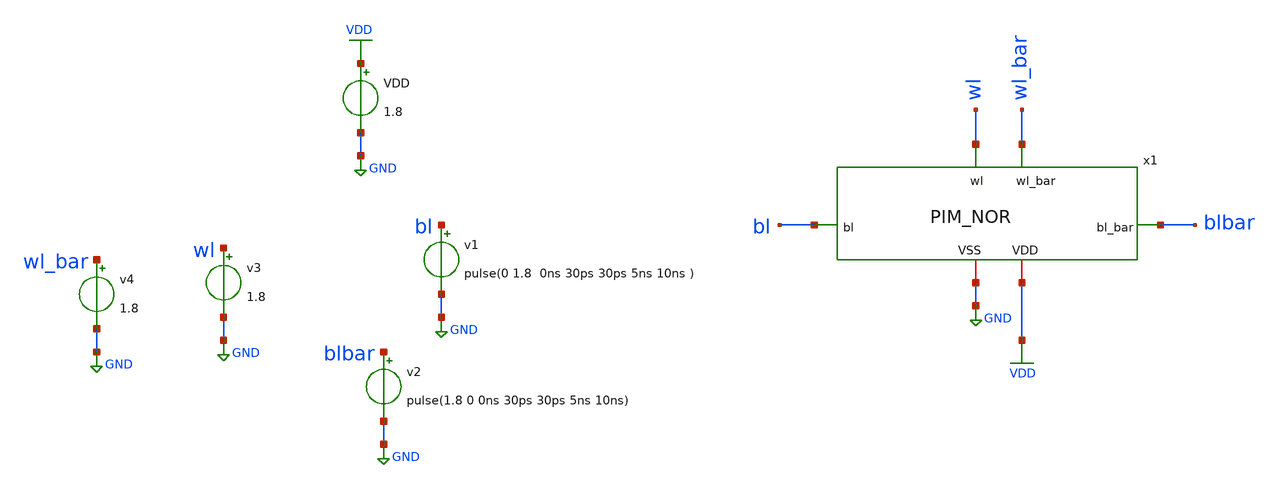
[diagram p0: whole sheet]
** sch_path: nikhil/SRAM/6T_PIM_TEST_SYMBOL.sch
**.subckt 6T_PIM_TEST_SYMBOL
x1 wl wl_bar VDD bl blbar GND PIM_NOR
VDD VDD GND 1.8
v1 bl GND pulse(0 1.8 0ns 30ps 30ps 5ns 10ns )
v3 wl GND 1.8
v2 blbar GND pulse(1.8 0 0ns 30ps 30ps 5ns 10ns)
v4 wl_bar GND 1.8
**** begin user architecture code

.tran


.options wnflag=1
.include /pdk/open_pdks/sources/sky130-pdk/libraries/sky130_fd_pr/latest/cells/nfet_01v8/sky130_fd_pr__nfet_01v8__tt.corner.spice
.include /pdk/open_pdks/sources/sky130-pdk/libraries/sky130_fd_pr/latest/cells/nfet_01v8_lvt/sky130_fd_pr__nfet_01v8_lvt__tt.corner.spice
.include /pdk/open_pdks/sources/sky130-pdk/libraries/sky130_fd_pr/latest/cells/pfet_01v8/sky130_fd_pr__pfet_01v8__tt.corner.spice
.include /pdk/open_pdks/sources/sky130-pdk/libraries/sky130_fd_pr/latest/cells/nfet_03v3_nvt/sky130_fd_pr__nfet_03v3_nvt__tt.corner.spice
.include /pdk/open_pdks/sources/sky130-pdk/libraries/sky130_fd_pr/latest/cells/nfet_05v0_nvt/sky130_fd_pr__nfet_05v0_nvt__tt.corner.spice
.include /pdk/open_pdks/sources/sky130-pdk/libraries/sky130_fd_pr/latest/cells/esd_nfet_01v8/sky130_fd_pr__esd_nfet_01v8__tt.corner.spice
.include /pdk/open_pdks/sources/sky130-pdk/libraries/sky130_fd_pr/latest/cells/pfet_01v8_lvt/sky130_fd_pr__pfet_01v8_lvt__tt.corner.spice
.include /pdk/open_pdks/sources/sky130-pdk/libraries/sky130_fd_pr/latest/cells/pfet_01v8_hvt/sky130_fd_pr__pfet_01v8_hvt__tt.corner.spice
.include /pdk/open_pdks/sources/sky130-pdk/libraries/sky130_fd_pr/latest/cells/esd_pfet_g5v0d10v5/sky130_fd_pr__esd_pfet_g5v0d10v5__tt.corner.spice
.include /pdk/open_pdks/sources/sky130-pdk/libraries/sky130_fd_pr/latest/cells/pfet_g5v0d10v5/sky130_fd_pr__pfet_g5v0d10v5__tt.corner.spice
.include /pdk/open_pdks/sources/sky130-pdk/libraries/sky130_fd_pr/latest/cells/pfet_g5v0d16v0/sky130_fd_pr__pfet_g5v0d16v0__tt.corner.spice
.include /pdk/open_pdks/sources/sky130-pdk/libraries/sky130_fd_pr/latest/cells/nfet_g5v0d10v5/sky130_fd_pr__nfet_g5v0d10v5__tt.corner.spice
.include /pdk/open_pdks/sources/sky130-pdk/libraries/sky130_fd_pr/latest/cells/nfet_g5v0d16v0/sky130_fd_pr__nfet_g5v0d16v0__tt_discrete.corner.spice
.include /pdk/open_pdks/sources/sky130-pdk/libraries/sky130_fd_pr/latest/cells/esd_nfet_g5v0d10v5/sky130_fd_pr__esd_nfet_g5v0d10v5__tt.corner.spice
.include /pdk/open_pdks/sources/sky130-pdk/libraries/sky130_fd_pr/latest/models/corners/tt/nonfet.spice
* Mismatch parameters
.include /pdk/open_pdks/sources/sky130-pdk/libraries/sky130_fd_pr/latest/cells/nfet_01v8/sky130_fd_pr__nfet_01v8__mismatch.corner.spice
.include /pdk/open_pdks/sources/sky130-pdk/libraries/sky130_fd_pr/latest/cells/pfet_01v8/sky130_fd_pr__pfet_01v8__mismatch.corner.spice
.include /pdk/open_pdks/sources/sky130-pdk/libraries/sky130_fd_pr/latest/cells/nfet_01v8_lvt/sky130_fd_pr__nfet_01v8_lvt__mismatch.corner.spice
.include /pdk/open_pdks/sources/sky130-pdk/libraries/sky130_fd_pr/latest/cells/pfet_01v8_lvt/sky130_fd_pr__pfet_01v8_lvt__mismatch.corner.spice
.include /pdk/open_pdks/sources/sky130-pdk/libraries/sky130_fd_pr/latest/cells/pfet_01v8_hvt/sky130_fd_pr__pfet_01v8_hvt__mismatch.corner.spice
.include /pdk/open_pdks/sources/sky130-pdk/libraries/sky130_fd_pr/latest/cells/nfet_g5v0d10v5/sky130_fd_pr__nfet_g5v0d10v5__mismatch.corner.spice
.include /pdk/open_pdks/sources/sky130-pdk/libraries/sky130_fd_pr/latest/cells/pfet_g5v0d10v5/sky130_fd_pr__pfet_g5v0d10v5__mismatch.corner.spice
.include /pdk/open_pdks/sources/sky130-pdk/libraries/sky130_fd_pr/latest/cells/nfet_05v0_nvt/sky130_fd_pr__nfet_05v0_nvt__mismatch.corner.spice
.include /pdk/open_pdks/sources/sky130-pdk/libraries/sky130_fd_pr/latest/cells/nfet_03v3_nvt/sky130_fd_pr__nfet_03v3_nvt__mismatch.corner.spice
* Resistor$::SKYWATER_MODELS/Capacitor
.include /pdk/open_pdks/sources/sky130-pdk/libraries/sky130_fd_pr/latest/models/r+c/res_typical__cap_typical.spice
.include /pdk/open_pdks/sources/sky130-pdk/libraries/sky130_fd_pr/latest/models/r+c/res_typical__cap_typical__lin.spice
* Special cells
.include /pdk/open_pdks/sources/sky130-pdk/libraries/sky130_fd_pr/latest/models/corners/tt/specialized_cells.spice
* All models
.include /pdk/open_pdks/sources/sky130-pdk/libraries/sky130_fd_pr/latest/models/all.spice
* Corner
.include /pdk/open_pdks/sources/sky130-pdk/libraries/sky130_fd_pr/latest/models/corners/tt/rf.spice

**** end user architecture code
**.ends

* expanding   symbol:  SRAM/PIM_NOR.sym # of pins=6
** sym_path: nikhil/SRAM/PIM_NOR.sym
** sch_path: nikhil/SRAM/PIM_NOR.sch
.subckt PIM_NOR wl wl_bar VDD bl bl_bar VSS
*.ipin bl
*.ipin wl
*.iopin VSS
*.iopin VDD
*.ipin wl_bar
*.ipin bl_bar
XM2 Qbar Q VSS VSS sky130_fd_pr__nfet_01v8 L=0.15 W=0.36 nf=1 ad='int((nf+1)/2) * W/nf * 0.29' as='int((nf+2)/2) * W/nf * 0.29'
+ pd='2*int((nf+1)/2) * (W/nf + 0.29)' ps='2*int((nf+2)/2) * (W/nf + 0.29)' nrd='0.29 / W' nrs='0.29 / W'
+ sa=0 sb=0 sd=0 mult=1 m=1
XM3 Q Qbar VDD VDD sky130_fd_pr__pfet_01v8 L=0.15 W=0.42 nf=1 ad='int((nf+1)/2) * W/nf * 0.29' as='int((nf+2)/2) * W/nf * 0.29'
+ pd='2*int((nf+1)/2) * (W/nf + 0.29)' ps='2*int((nf+2)/2) * (W/nf + 0.29)' nrd='0.29 / W' nrs='0.29 / W'
+ sa=0 sb=0 sd=0 mult=1 m=1
XM4 Qbar Q VDD VDD sky130_fd_pr__pfet_01v8 L=0.15 W=0.42 nf=1 ad='int((nf+1)/2) * W/nf * 0.29' as='int((nf+2)/2) * W/nf * 0.29'
+ pd='2*int((nf+1)/2) * (W/nf + 0.29)' ps='2*int((nf+2)/2) * (W/nf + 0.29)' nrd='0.29 / W' nrs='0.29 / W'
+ sa=0 sb=0 sd=0 mult=1 m=1
XM5 bl wl Q GND sky130_fd_pr__nfet_01v8 L=0.15 W=0.36 nf=1 ad='int((nf+1)/2) * W/nf * 0.29' as='int((nf+2)/2) * W/nf * 0.29'
+ pd='2*int((nf+1)/2) * (W/nf + 0.29)' ps='2*int((nf+2)/2) * (W/nf + 0.29)' nrd='0.29 / W' nrs='0.29 / W'
+ sa=0 sb=0 sd=0 mult=1 m=1
XM6 bl_bar wl_bar Qbar GND sky130_fd_pr__nfet_01v8 L=0.15 W=0.36 nf=1 ad='int((nf+1)/2) * W/nf * 0.29'
+ as='int((nf+2)/2) * W/nf * 0.29' pd='2*int((nf+1)/2) * (W/nf + 0.29)' ps='2*int((nf+2)/2) * (W/nf + 0.29)'
+ nrd='0.29 / W' nrs='0.29 / W' sa=0 sb=0 sd=0 mult=1 m=1
XM1 Q Qbar VSS VSS sky130_fd_pr__nfet_01v8 L=0.15 W=0.36 nf=1 ad='int((nf+1)/2) * W/nf * 0.29' as='int((nf+2)/2) * W/nf * 0.29'
+ pd='2*int((nf+1)/2) * (W/nf + 0.29)' ps='2*int((nf+2)/2) * (W/nf + 0.29)' nrd='0.29 / W' nrs='0.29 / W'
+ sa=0 sb=0 sd=0 mult=1 m=1
.ends

.GLOBAL GND
.GLOBAL VDD
.end
